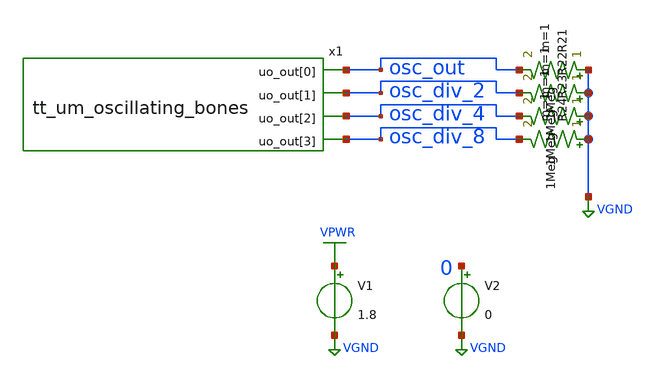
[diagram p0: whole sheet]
** sch_path: xschem/testbench.sch
**.subckt testbench
x1 osc_out osc_div_2 osc_div_4 osc_div_8 tt_um_oscillating_bones
V1 VPWR VGND 1.8
R21 VGND osc_out 1Meg m=1
R22 VGND osc_div_2 1Meg m=1
R23 VGND osc_div_4 1Meg m=1
R24 VGND osc_div_8 1Meg m=1
V2 0 VGND 0
**** begin user architecture code

** opencircuitdesign pdks install
.lib $::SKYWATER_MODELS/sky130.lib.spice tt
.include $::SKYWATER_STDCELLS/sky130_fd_sc_hd.spice





.tran 50p 200n
.save all

.control
run

meas tran tdiff TRIG osc_out VAL=1.7 RISE=2 TARG osc_out VAL=1.7 RISE=3
let osc_freq_mhz = (1 / (tdiff) / 1e6)
save osc_freq_mhz

meas tran tdiff_div2 TRIG osc_div_2 VAL=1.7 RISE=2 TARG osc_div_2 VAL=1.7 RISE=3
let osc_div_2_freq_mhz = (1 / (tdiff_div2) / 1e6)
save osc_div_2_freq_mhz

meas tran tdiff_div4 TRIG osc_div_4 VAL=1.7 RISE=2 TARG osc_div_4 VAL=1.7 RISE=3
let osc_div_4_freq_mhz = (1 / (tdiff_div4) / 1e6)
save osc_div_4_freq_mhz

meas tran tdiff_div8 TRIG osc_div_8 VAL=1.7 RISE=2 TARG osc_div_8 VAL=1.7 RISE=3
let osc_div_8_freq_mhz = (1 / (tdiff_div8) / 1e6)
save osc_div_8_freq_mhz

write testbench.raw
.endc


**** end user architecture code
**.ends

* expanding   symbol:  tt_um_oscillating_bones.sym # of pins=4
** sym_path: xschem/tt_um_oscillating_bones.sym
** sch_path: xschem/tt_um_oscillating_bones.sch
.subckt tt_um_oscillating_bones uo_out[0] uo_out[1] uo_out[2] uo_out[3]
*.opin uo_out[1]
*.opin uo_out[0]
*.opin uo_out[2]
*.opin uo_out[3]
x22 uo_out[1] uo_out[2] uo_out[3] uo_out[0] freq_divider
x1 uo_out[0] ring
.ends


* expanding   symbol:  freq_divider.sym # of pins=4
** sym_path: xschem/freq_divider.sym
** sch_path: xschem/freq_divider.sch
.subckt freq_divider ODIV2 ODIV4 ODIV8 IN
*.ipin IN
*.opin ODIV2
*.opin ODIV4
*.opin ODIV8
x1 IN net3 VGND VNB VPB VPWR ODIV2 net3 sky130_fd_sc_hd__dfxbp_1
x2 ODIV2 net1 VGND VNB VPB VPWR ODIV4 net1 sky130_fd_sc_hd__dfxbp_1
x3 ODIV4 net2 VGND VNB VPB VPWR ODIV8 net2 sky130_fd_sc_hd__dfxbp_1
.ends


* expanding   symbol:  ring.sym # of pins=1
** sym_path: xschem/ring.sym
** sch_path: xschem/ring.sch
.subckt ring ROSC_OUT
*.opin ROSC_OUT
x1 net20 net1 skullfet_inverter
x2 net1 net3 skullfet_inverter
x3 net3 net2 skullfet_inverter
x4 net2 ROSC_OUT skullfet_inverter
x5 ROSC_OUT net4 skullfet_inverter
x7 net5 net6 skullfet_inverter
x6 net4 net5 skullfet_inverter
x8 net6 net7 skullfet_inverter
x9 net7 net11 skullfet_inverter
x10 net11 net8 skullfet_inverter
x11 net8 net9 skullfet_inverter
x12 net9 net10 skullfet_inverter
x13 net10 net12 skullfet_inverter
x14 net12 net13 skullfet_inverter
x15 net13 net14 skullfet_inverter
x16 net14 net15 skullfet_inverter
x17 net15 net16 skullfet_inverter
x18 net16 net17 skullfet_inverter
x19 net17 net18 skullfet_inverter
x20 net18 net19 skullfet_inverter
x21 net19 net20 skullfet_inverter
.ends


* expanding   symbol:  skullfet_inverter.sym # of pins=2
** sym_path: xschem/skullfet_inverter.sym
** sch_path: xschem/skullfet_inverter.sch
.subckt skullfet_inverter A Y
*.ipin A
*.opin Y
XM1 Y A VPWR VPWR sky130_fd_pr__pfet_01v8_hvt L=0.4 W=4.05 nf=1 ad=6.2694 as=4.4307 pd=26.64 ps=10.9
+ nrd='0.29 / 4.05 ' nrs='0.29 / 4.05 ' sa=0 sb=0 sd=0 mult=1 m=1
XM2 Y A VGND VGND sky130_fd_pr__nfet_01v8 L=0.4 W=4.05 nf=1 ad=4.2687 as=6.4314 pd=10.82 ps=26.72 nrd='0.29 / 4.05 '
+ nrs='0.29 / 4.05 ' sa=0 sb=0 sd=0 mult=1 m=1
.ends

.GLOBAL VGND
.GLOBAL VPWR
.end
